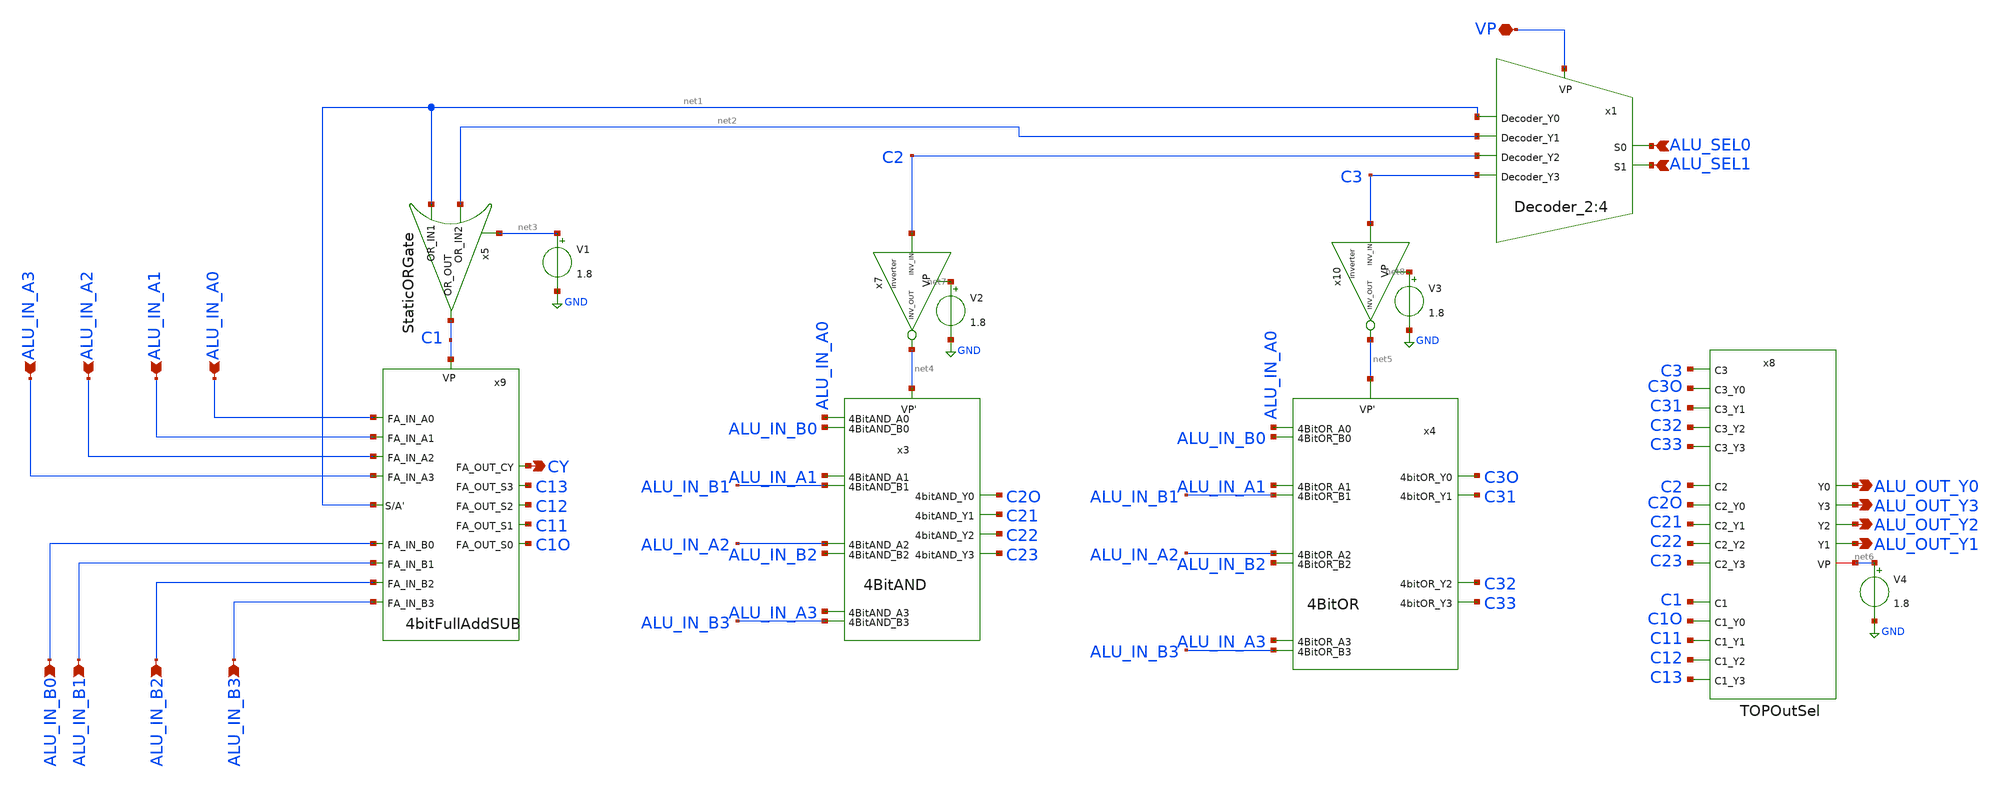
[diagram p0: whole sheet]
** sch_path: ALU_TOP_MODEL/ALU.sch
**.subckt ALU VP ALU_OUT_Y0 ALU_OUT_Y3 ALU_OUT_Y1 ALU_OUT_Y2 CY ALU_IN_A0 ALU_IN_B0 ALU_IN_A1
*+ ALU_IN_B1 ALU_IN_A2 ALU_IN_B2 ALU_IN_A3 ALU_IN_B3 ALU_SEL0 ALU_SEL1
*.iopin VP
*.opin ALU_OUT_Y0
*.opin ALU_OUT_Y3
*.opin ALU_OUT_Y1
*.opin ALU_OUT_Y2
*.opin CY
*.ipin ALU_IN_A0
*.ipin ALU_IN_B0
*.ipin ALU_IN_A1
*.ipin ALU_IN_B1
*.ipin ALU_IN_A2
*.ipin ALU_IN_B2
*.ipin ALU_IN_A3
*.ipin ALU_IN_B3
*.ipin ALU_SEL0
*.ipin ALU_SEL1
V1 net3 GND 1.8
x8 C3 C33 C31 C3O C32 C22 C23 C2O C21 ALU_OUT_Y0 ALU_OUT_Y3 ALU_OUT_Y2 ALU_OUT_Y1 C12 C13 C11 C1O C1
+ net6 C2 TOPOutSel
V2 net7 GND 1.8
V3 net8 GND 1.8
V4 net6 GND 1.8
x5 net2 net1 C1 net3 StaticORGate
x9 ALU_IN_A1 ALU_IN_B1 ALU_IN_B2 ALU_IN_B3 ALU_IN_A3 ALU_IN_A2 ALU_IN_B0 ALU_IN_A0 C1 CY C13 C12 C11
+ C1O net1 4bitFullAddSUB
x3 ALU_IN_A0 C2O ALU_IN_B0 ALU_IN_A1 C21 ALU_IN_B1 ALU_IN_A2 C22 ALU_IN_B2 ALU_IN_A3 C23 ALU_IN_B3
+ net4 4BitAND
x4 ALU_IN_A0 C3O ALU_IN_B0 ALU_IN_A1 C31 ALU_IN_B1 ALU_IN_A2 C32 ALU_IN_B2 ALU_IN_A3 C33 ALU_IN_B3
+ net5 4BitOR
x7 net7 net4 C2 inverter
x10 net8 net5 C3 inverter
x1 ALU_SEL0 ALU_SEL1 net1 VP net2 C2 C3 Decoder_2:4
**.ends
.GLOBAL GND
.end
